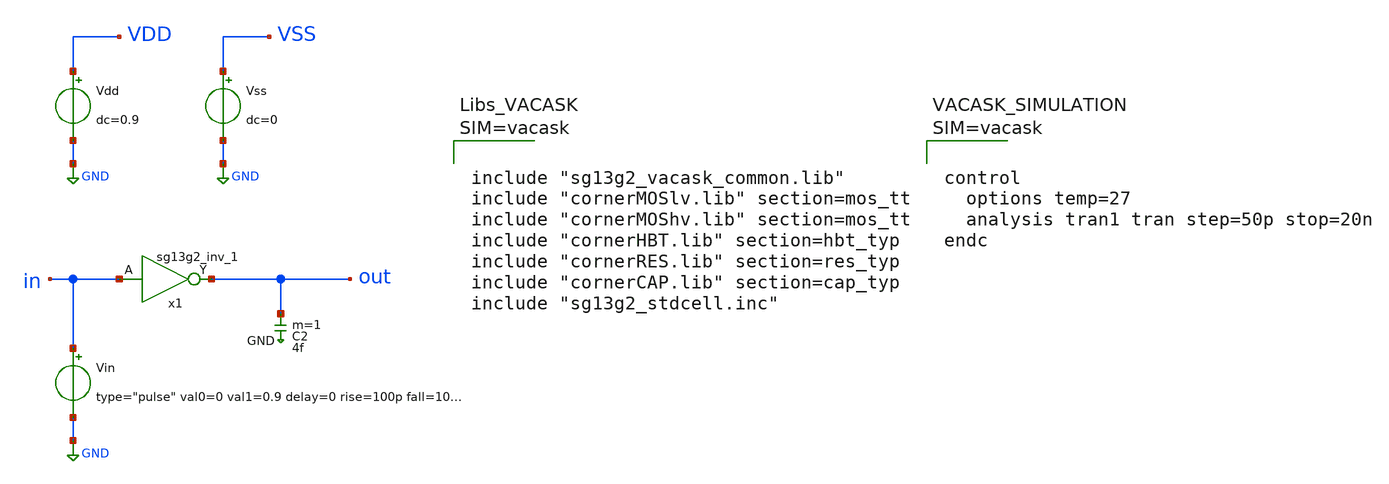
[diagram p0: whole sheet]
** sch_path: demo/ihp-sg13g2/tran_inv.sch
* Copyright 2024 IHP PDK Authors
**.subckt tran_inv
Vin in GND type="pulse" val0=0 val1=0.9 delay=0 rise=100p fall=100p width=2n period=4n
x1 out in VDD VSS sg13g2_inv_1
C2 out GND 4f m=1
Vdd VDD GND dc=0.9
Vss VSS GND dc=0
**** begin user architecture code






**** end user architecture code
**.ends

* expanding   symbol:  sg13g2_stdcells/sg13g2_inv_1.sym # of pins=2
** sym_path: sg13g2_stdcells/sg13g2_inv_1.sym
** sch_path: sg13g2_stdcells/sg13g2_inv_1.sch
.subckt sg13g2_inv_1 Y A VDD VSS
*.opin Y
*.ipin A
*.iopin VDD
*.iopin VSS
XM1 Y A VSS VSS sg13_lv_nmos w=740.00n l=130.00n ng=1 m=1 mm_ok=1
XM2 Y A VDD VDD sg13_lv_pmos w=1.12u l=130.00n ng=1 m=1 mm_ok=1
.ends

.GLOBAL GND
.end
